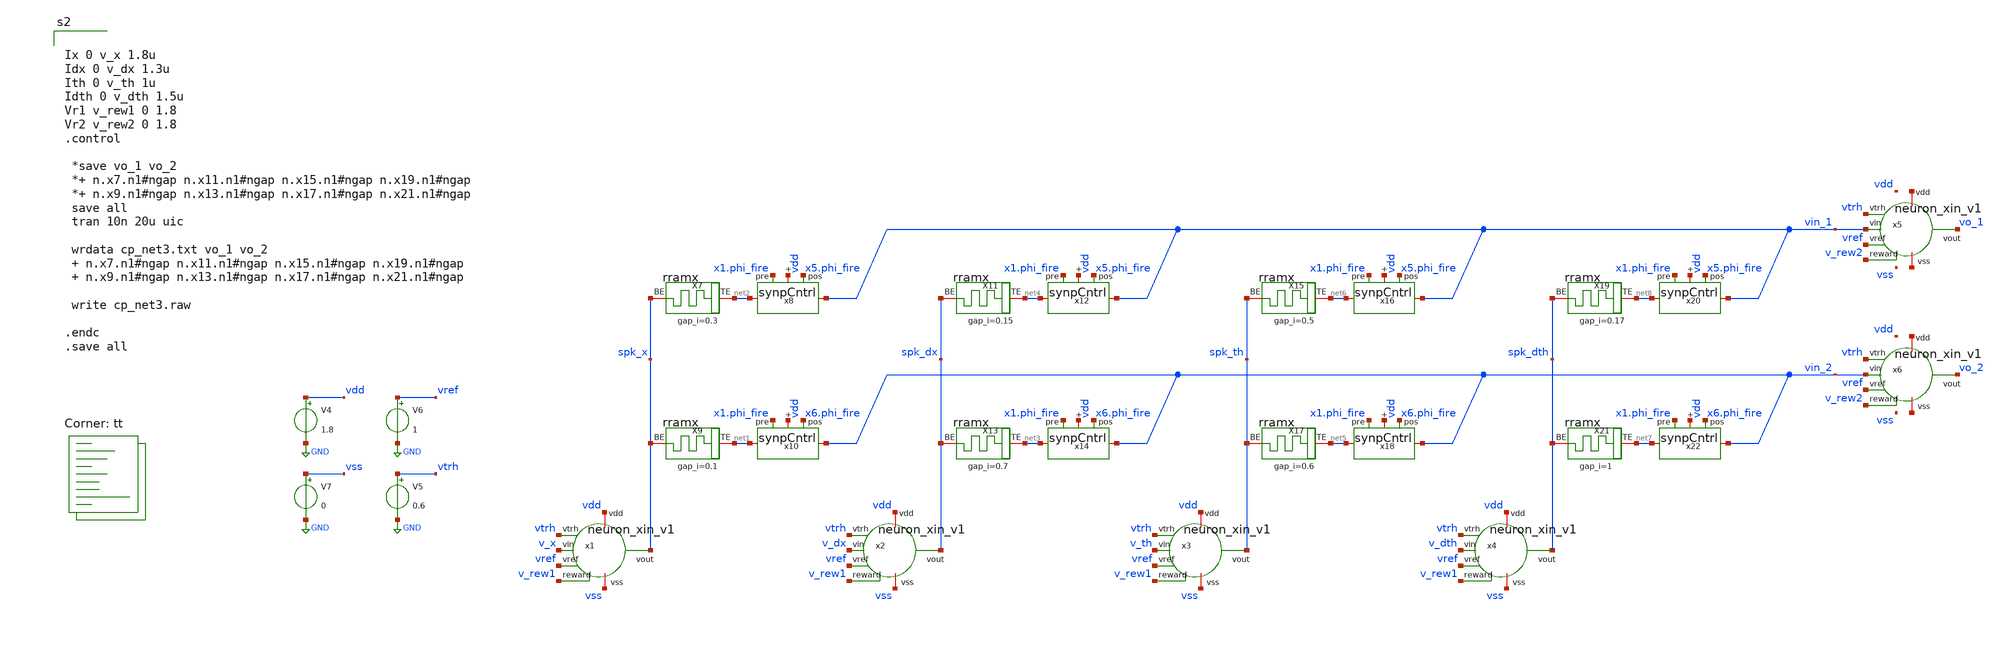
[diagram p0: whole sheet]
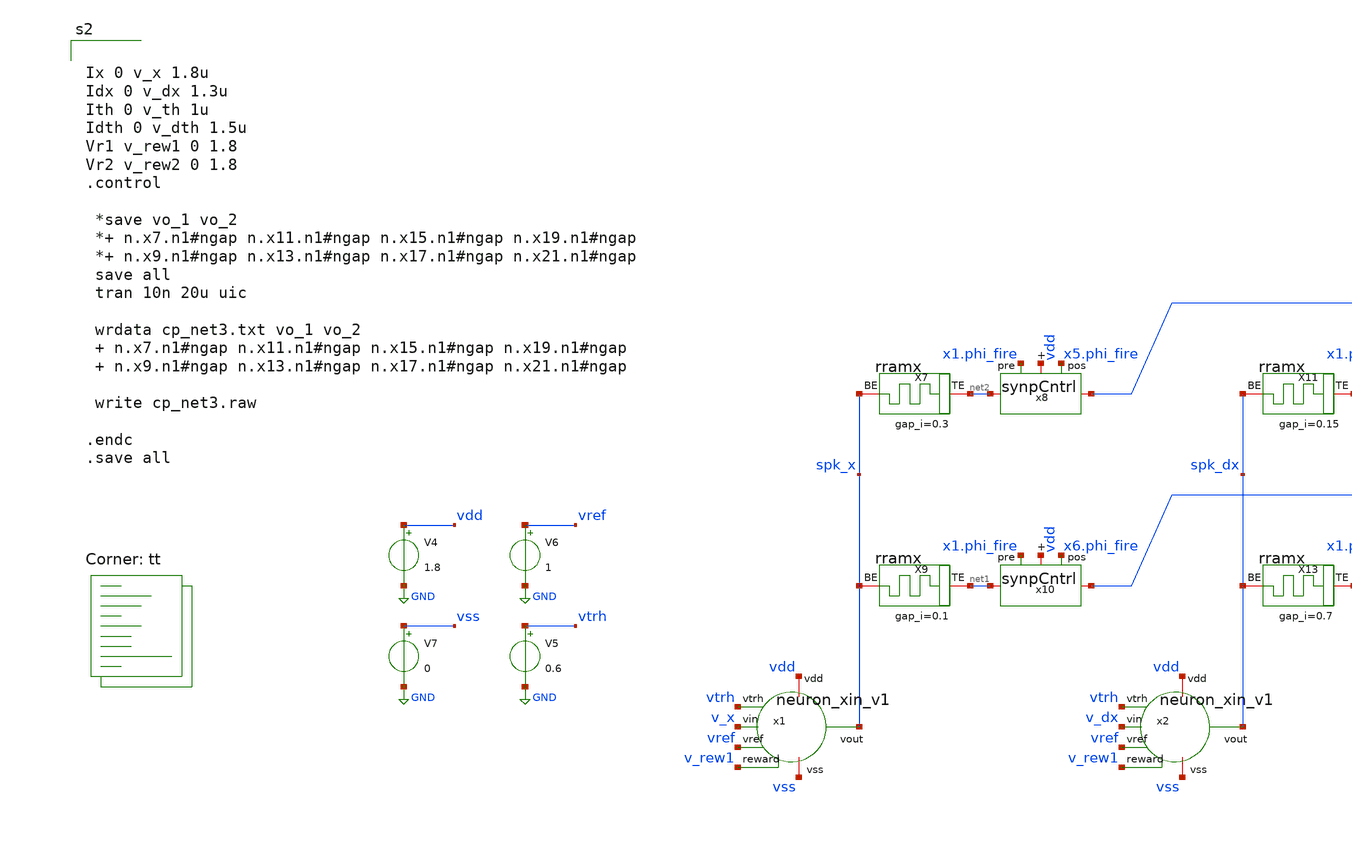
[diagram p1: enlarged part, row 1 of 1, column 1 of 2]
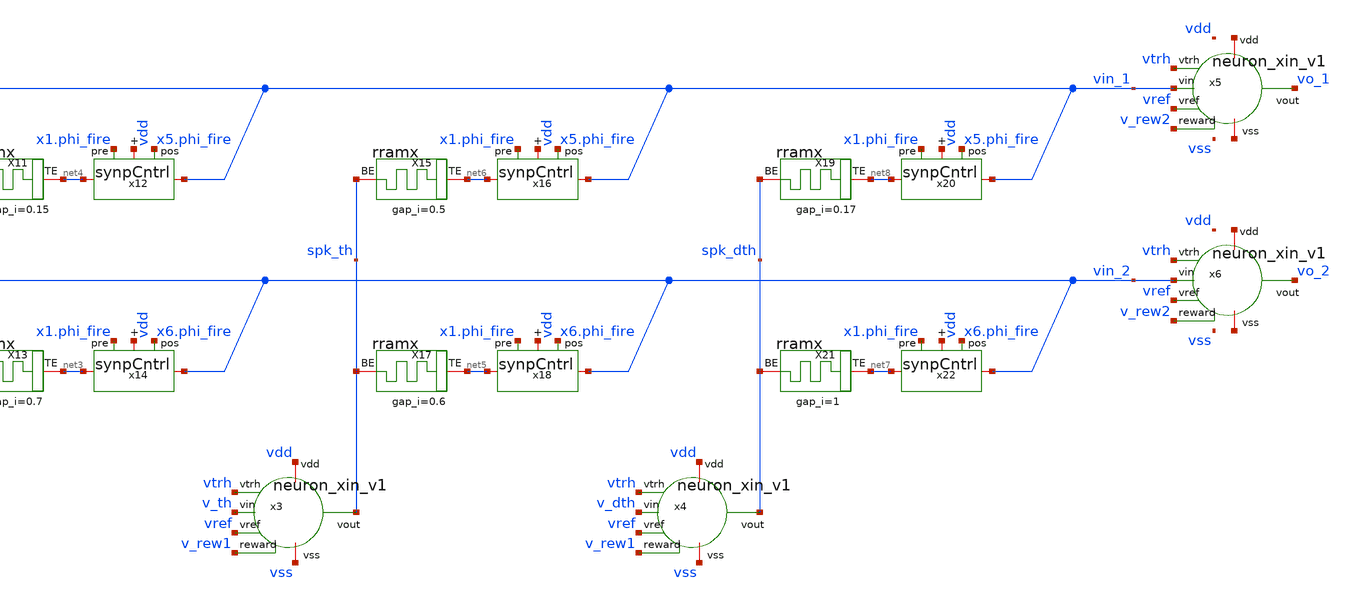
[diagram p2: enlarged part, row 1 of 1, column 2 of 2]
** sch_path: tests/cp_net3.sch
**.subckt cp_net3
V4 vdd GND 1.8
V5 vtrh GND 0.6
V6 vref GND 1
V7 vss GND 0
x1 vdd vss spk_x v_x vtrh vref v_rew1 neuron_xin_v1
x2 vdd vss spk_dx v_dx vtrh vref v_rew1 neuron_xin_v1
x3 vdd vss spk_th v_th vtrh vref v_rew1 neuron_xin_v1
x4 vdd vss spk_dth v_dth vtrh vref v_rew1 neuron_xin_v1
x5 net9 net10 vo_1 vin_1 vtrh vref v_rew2 neuron_xin_v1
x6 net11 net12 vo_2 vin_2 vtrh vref v_rew2 neuron_xin_v1
X13 net3 spk_dx rram_cell gap_i=0.7
X17 net5 spk_th rram_cell gap_i=0.6
X9 net1 spk_x rram_cell gap_i=0.1
x10 vdd x1.phi_fire x6.phi_fire net1 vin_2 synpCntrl
X21 net7 spk_dth rram_cell gap_i=1
X11 net4 spk_dx rram_cell gap_i=0.15
X15 net6 spk_th rram_cell gap_i=0.5
X7 net2 spk_x rram_cell gap_i=0.3
X19 net8 spk_dth rram_cell gap_i=0.17
x8 vdd x1.phi_fire x5.phi_fire net2 vin_1 synpCntrl
x14 vdd x1.phi_fire x6.phi_fire net3 vin_2 synpCntrl
x12 vdd x1.phi_fire x5.phi_fire net4 vin_1 synpCntrl
x18 vdd x1.phi_fire x6.phi_fire net5 vin_2 synpCntrl
x16 vdd x1.phi_fire x5.phi_fire net6 vin_1 synpCntrl
x22 vdd x1.phi_fire x6.phi_fire net7 vin_2 synpCntrl
x20 vdd x1.phi_fire x5.phi_fire net8 vin_1 synpCntrl
**** begin user architecture code


Ix 0 v_x 1.8u
Idx 0 v_dx 1.3u
Ith 0 v_th 1u
Idth 0 v_dth 1.5u
Vr1 v_rew1 0 1.8
Vr2 v_rew2 0 1.8
.control

 *save vo_1 vo_2
 *+ n.x7.n1#ngap n.x11.n1#ngap n.x15.n1#ngap n.x19.n1#ngap
 *+ n.x9.n1#ngap n.x13.n1#ngap n.x17.n1#ngap n.x21.n1#ngap
 save all
 tran 10n 20u uic

 wrdata cp_net3.txt vo_1 vo_2
 + n.x7.n1#ngap n.x11.n1#ngap n.x15.n1#ngap n.x19.n1#ngap
 + n.x9.n1#ngap n.x13.n1#ngap n.x17.n1#ngap n.x21.n1#ngap

 write cp_net3.raw

.endc
.save all


.lib $::SKYWATER_MODELS/sky130.lib.spice tt

.subckt rram_cell BE TE gap_i=0.1
N1 BE TE rram_model
.model rram_model rram gap_initial={gap_i}
.ends rram_cell

.control
pre_osdi /foss/designs/spike_130/designs/prubs/rram.osdi
.endc

**** end user architecture code
**.ends
.GLOBAL GND
.end
